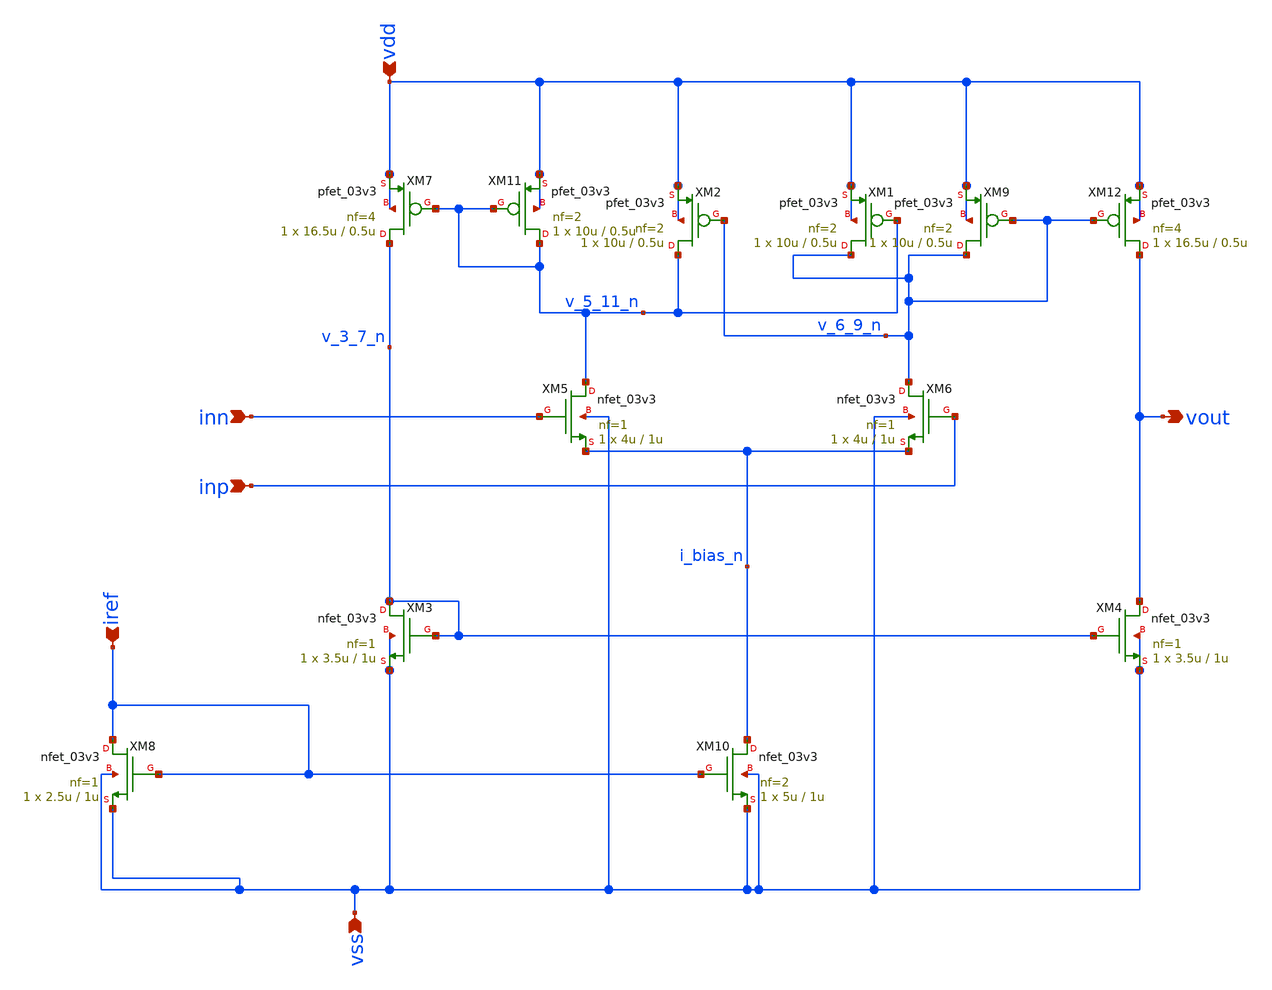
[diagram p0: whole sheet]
** sch_path: designs/libs/core_analog/Comparator/Nmos_Comparator.sch
**.subckt Nmos_Comparator vss vdd iref inn inp vout
*.ipin vss
*.ipin vdd
*.ipin iref
*.ipin inn
*.ipin inp
*.opin vout
XM3 v_3_7_n v_3_7_n vss vss nfet_03v3 L=1u W=3.5u nf=1 ad='int((nf+1)/2) * W/nf * 0.18u' as='int((nf+2)/2) * W/nf * 0.18u'
+ pd='2*int((nf+1)/2) * (W/nf + 0.18u)' ps='2*int((nf+2)/2) * (W/nf + 0.18u)' nrd='0.18u / W' nrs='0.18u / W'
+ sa=0 sb=0 sd=0 m=1
XM4 vout v_3_7_n vss vss nfet_03v3 L=1u W=3.5u nf=1 ad='int((nf+1)/2) * W/nf * 0.18u' as='int((nf+2)/2) * W/nf * 0.18u'
+ pd='2*int((nf+1)/2) * (W/nf + 0.18u)' ps='2*int((nf+2)/2) * (W/nf + 0.18u)' nrd='0.18u / W' nrs='0.18u / W'
+ sa=0 sb=0 sd=0 m=1
XM5 v_5_11_n inn i_bias_n vss nfet_03v3 L=1u W=4u nf=1 ad='int((nf+1)/2) * W/nf * 0.18u' as='int((nf+2)/2) * W/nf * 0.18u'
+ pd='2*int((nf+1)/2) * (W/nf + 0.18u)' ps='2*int((nf+2)/2) * (W/nf + 0.18u)' nrd='0.18u / W' nrs='0.18u / W'
+ sa=0 sb=0 sd=0 m=1
XM6 v_6_9_n inp i_bias_n vss nfet_03v3 L=1u W=4u nf=1 ad='int((nf+1)/2) * W/nf * 0.18u' as='int((nf+2)/2) * W/nf * 0.18u'
+ pd='2*int((nf+1)/2) * (W/nf + 0.18u)' ps='2*int((nf+2)/2) * (W/nf + 0.18u)' nrd='0.18u / W' nrs='0.18u / W'
+ sa=0 sb=0 sd=0 m=1
XM7 v_3_7_n v_5_11_n vdd vdd pfet_03v3 L=0.5u W=16.5u nf=4 ad='int((nf+1)/2) * W/nf * 0.18u' as='int((nf+2)/2) * W/nf * 0.18u'
+ pd='2*int((nf+1)/2) * (W/nf + 0.18u)' ps='2*int((nf+2)/2) * (W/nf + 0.18u)' nrd='0.18u / W' nrs='0.18u / W'
+ sa=0 sb=0 sd=0 m=1
XM9 v_6_9_n v_6_9_n vdd vdd pfet_03v3 L=0.5u W=10u nf=2 ad='int((nf+1)/2) * W/nf * 0.18u' as='int((nf+2)/2) * W/nf * 0.18u'
+ pd='2*int((nf+1)/2) * (W/nf + 0.18u)' ps='2*int((nf+2)/2) * (W/nf + 0.18u)' nrd='0.18u / W' nrs='0.18u / W'
+ sa=0 sb=0 sd=0 m=1
XM11 v_5_11_n v_5_11_n vdd vdd pfet_03v3 L=0.5u W=10u nf=2 ad='int((nf+1)/2) * W/nf * 0.18u' as='int((nf+2)/2) * W/nf * 0.18u'
+ pd='2*int((nf+1)/2) * (W/nf + 0.18u)' ps='2*int((nf+2)/2) * (W/nf + 0.18u)' nrd='0.18u / W' nrs='0.18u / W'
+ sa=0 sb=0 sd=0 m=1
XM12 vout v_6_9_n vdd vdd pfet_03v3 L=0.5u W=16.5u nf=4 ad='int((nf+1)/2) * W/nf * 0.18u' as='int((nf+2)/2) * W/nf * 0.18u'
+ pd='2*int((nf+1)/2) * (W/nf + 0.18u)' ps='2*int((nf+2)/2) * (W/nf + 0.18u)' nrd='0.18u / W' nrs='0.18u / W'
+ sa=0 sb=0 sd=0 m=1
XM1 v_6_9_n v_5_11_n vdd vdd pfet_03v3 L=0.5u W=10u nf=2 ad='int((nf+1)/2) * W/nf * 0.18u' as='int((nf+2)/2) * W/nf * 0.18u'
+ pd='2*int((nf+1)/2) * (W/nf + 0.18u)' ps='2*int((nf+2)/2) * (W/nf + 0.18u)' nrd='0.18u / W' nrs='0.18u / W'
+ sa=0 sb=0 sd=0 m=1
XM2 v_5_11_n v_6_9_n vdd vdd pfet_03v3 L=0.5u W=10u nf=2 ad='int((nf+1)/2) * W/nf * 0.18u' as='int((nf+2)/2) * W/nf * 0.18u'
+ pd='2*int((nf+1)/2) * (W/nf + 0.18u)' ps='2*int((nf+2)/2) * (W/nf + 0.18u)' nrd='0.18u / W' nrs='0.18u / W'
+ sa=0 sb=0 sd=0 m=1
XM8 iref iref vss vss nfet_03v3 L=1u W=2.5u nf=1 ad='int((nf+1)/2) * W/nf * 0.18u' as='int((nf+2)/2) * W/nf * 0.18u'
+ pd='2*int((nf+1)/2) * (W/nf + 0.18u)' ps='2*int((nf+2)/2) * (W/nf + 0.18u)' nrd='0.18u / W' nrs='0.18u / W'
+ sa=0 sb=0 sd=0 m=1
XM10 i_bias_n iref vss vss nfet_03v3 L=1u W=5u nf=2 ad='int((nf+1)/2) * W/nf * 0.18u' as='int((nf+2)/2) * W/nf * 0.18u'
+ pd='2*int((nf+1)/2) * (W/nf + 0.18u)' ps='2*int((nf+2)/2) * (W/nf + 0.18u)' nrd='0.18u / W' nrs='0.18u / W'
+ sa=0 sb=0 sd=0 m=1
**.ends
.end
